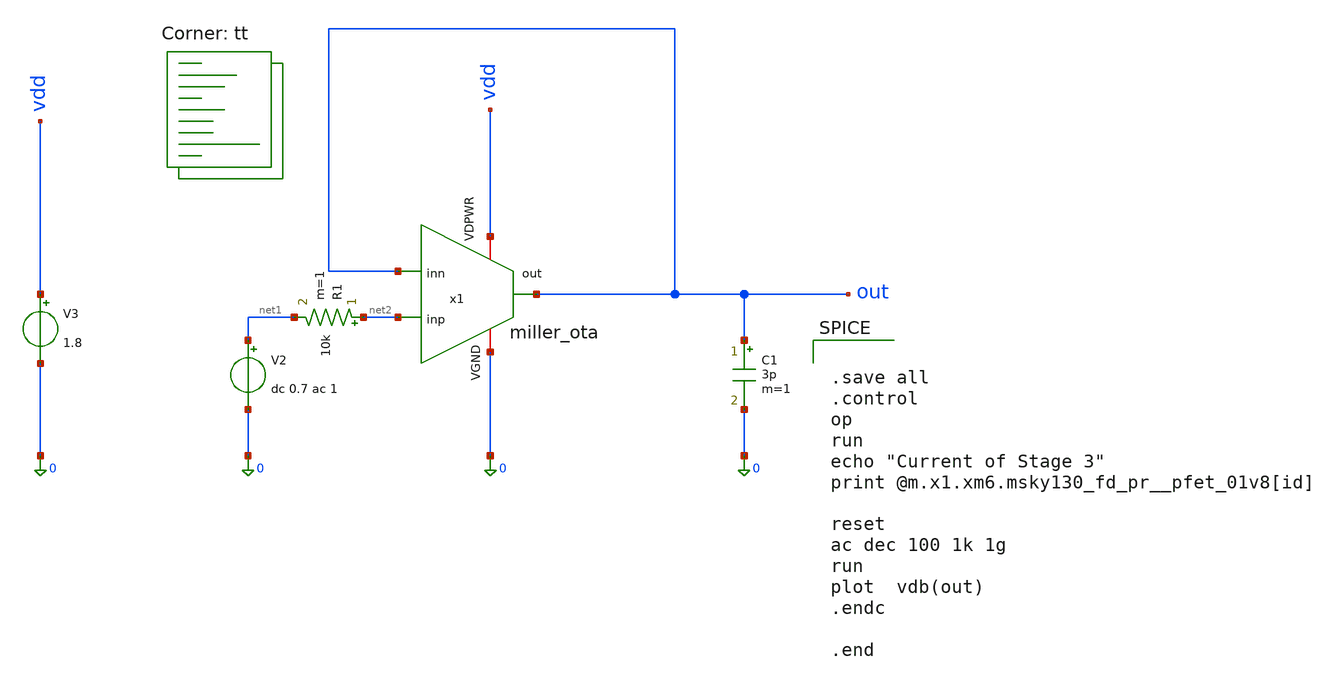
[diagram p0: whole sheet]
** sch_path: src/xschem/miller_ota_test_closedLoop.sch
**.subckt miller_ota_test_closedLoop
x1 vdd out out net2 0 miller_ota
V2 net1 0 dc 0.7 ac 1
R1 net2 net1 10k m=1
C1 out 0 3p m=1
V3 vdd 0 1.8
**** begin user architecture code


.save all
.control
op
run
echo "Current of Stage 3"
print @m.x1.xm6.msky130_fd_pr__pfet_01v8[id]

reset
ac dec 100 1k 1g
run
plot  vdb(out)
.endc

.end

.lib $::SKYWATER_MODELS/sky130.lib.spice tt
**** end user architecture code
**.ends
.end
